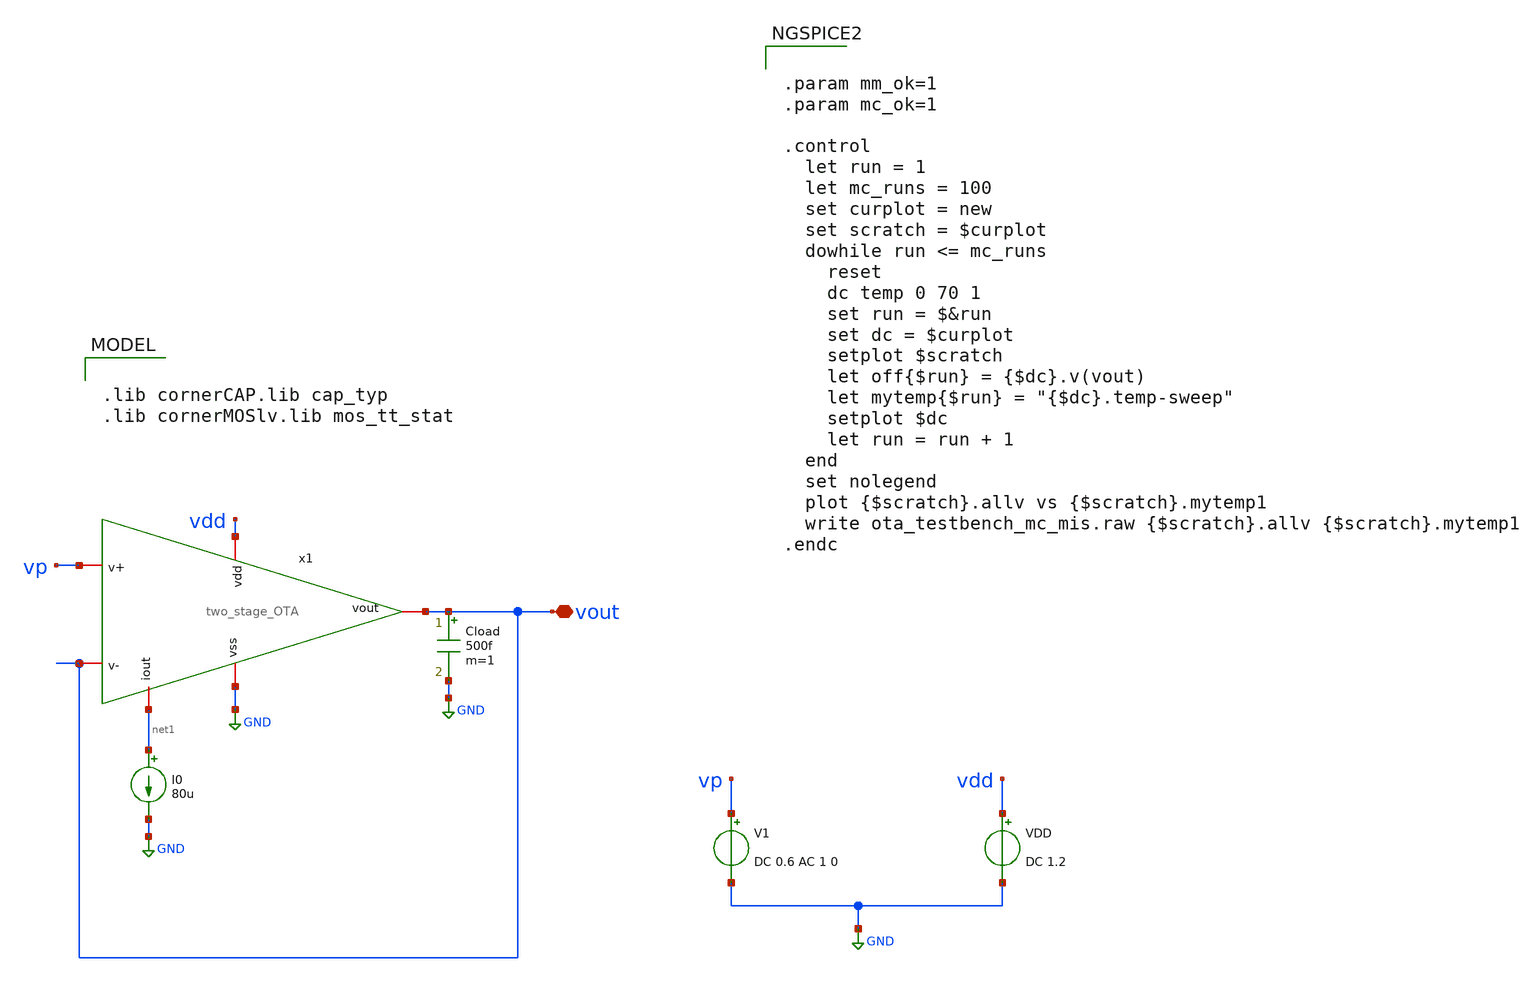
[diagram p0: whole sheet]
** sch_path: modules/module_1_bandgap_reference/part_1_OTA/testbenches/ota_testbench_mc_mis.sch
**.subckt ota_testbench_mc_mis vout
*.iopin vout
V1 vp GND DC 0.6 AC 1 0
VDD vdd GND DC 1.2
I0 net1 GND 80u
Cload vout GND 500f m=1
x1 vdd net1 vp vout vout GND two_stage_OTA
**** begin user architecture code

.lib cornerCAP.lib cap_typ
.lib cornerMOSlv.lib mos_tt_stat



.param mm_ok=1
.param mc_ok=1

.control
  let run = 1
  let mc_runs = 100
  set curplot = new
  set scratch = $curplot
  dowhile run <= mc_runs
    reset
    dc temp 0 70 1
    set run = $&run
    set dc = $curplot
    setplot $scratch
    let off{$run} = {$dc}.v(vout)
    let mytemp{$run} = "{$dc}.temp-sweep"
    setplot $dc
    let run = run + 1
  end
  set nolegend
  plot {$scratch}.allv vs {$scratch}.mytemp1
  write ota_testbench_mc_mis.raw {$scratch}.allv {$scratch}.mytemp1
.endc





**** end user architecture code
**.ends

* expanding   symbol:  two_stage_OTA.sym # of pins=6
** sym_path: modules/module_1_bandgap_reference/part_1_OTA/gmid_example/schematic/two_stage_OTA.sym
** sch_path: modules/module_1_bandgap_reference/part_1_OTA/gmid_example/schematic/two_stage_OTA.sch
.subckt two_stage_OTA vdd iout v+ v- vout vss
*.iopin v-
*.iopin v+
*.iopin vss
*.iopin vdd
*.iopin iout
*.iopin vout
XM4 vout net1 vss vss sg13_lv_nmos w=3.09u l=6.24u ng=1 m=1 mm_ok=1
XM3 net1 net1 vss vss sg13_lv_nmos w=3.09u l=6.24u ng=1 m=1 mm_ok=1
XM1 net1 v+ net2 vdd sg13_lv_pmos w=2.75u l=5.46u ng=1 m=1 mm_ok=1
XM5 net2 iout vdd vdd sg13_lv_pmos w=66u l=9.98u ng=10 m=1 mm_ok=1
XM6 iout iout vdd vdd sg13_lv_pmos w=66u l=9.98u ng=10 m=1 mm_ok=1
XM2 vout v- net2 vdd sg13_lv_pmos w=2.75u l=5.46u ng=1 m=1 mm_ok=1
.ends

.GLOBAL GND
.end
